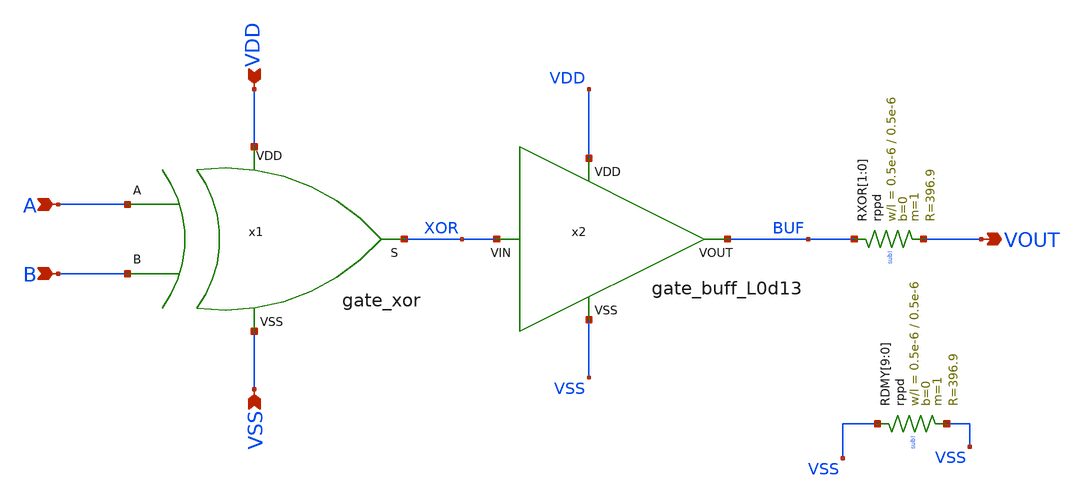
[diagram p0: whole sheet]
** sch_path: work/integrator_phasedetector/xschem/integrator_phasedetector.sch
**.subckt integrator_phasedetector A B VSS VDD VOUT
*.ipin A
*.ipin B
*.ipin VSS
*.ipin VDD
*.opin VOUT
x1 VDD XOR B A VSS gate_xor
x2 VDD XOR BUF VSS gate_buff_L0d13
XRXOR[1] BUF VOUT sub! rppd w=0.5e-6 l=0.5e-6 m=1 b=0 mm_ok=1
XRXOR[0] BUF VOUT sub! rppd w=0.5e-6 l=0.5e-6 m=1 b=0 mm_ok=1
XRDMY[9] VSS VSS sub! rppd w=0.5e-6 l=0.5e-6 m=1 b=0 mm_ok=1
XRDMY[8] VSS VSS sub! rppd w=0.5e-6 l=0.5e-6 m=1 b=0 mm_ok=1
XRDMY[7] VSS VSS sub! rppd w=0.5e-6 l=0.5e-6 m=1 b=0 mm_ok=1
XRDMY[6] VSS VSS sub! rppd w=0.5e-6 l=0.5e-6 m=1 b=0 mm_ok=1
XRDMY[5] VSS VSS sub! rppd w=0.5e-6 l=0.5e-6 m=1 b=0 mm_ok=1
XRDMY[4] VSS VSS sub! rppd w=0.5e-6 l=0.5e-6 m=1 b=0 mm_ok=1
XRDMY[3] VSS VSS sub! rppd w=0.5e-6 l=0.5e-6 m=1 b=0 mm_ok=1
XRDMY[2] VSS VSS sub! rppd w=0.5e-6 l=0.5e-6 m=1 b=0 mm_ok=1
XRDMY[1] VSS VSS sub! rppd w=0.5e-6 l=0.5e-6 m=1 b=0 mm_ok=1
XRDMY[0] VSS VSS sub! rppd w=0.5e-6 l=0.5e-6 m=1 b=0 mm_ok=1
**.ends
.end
